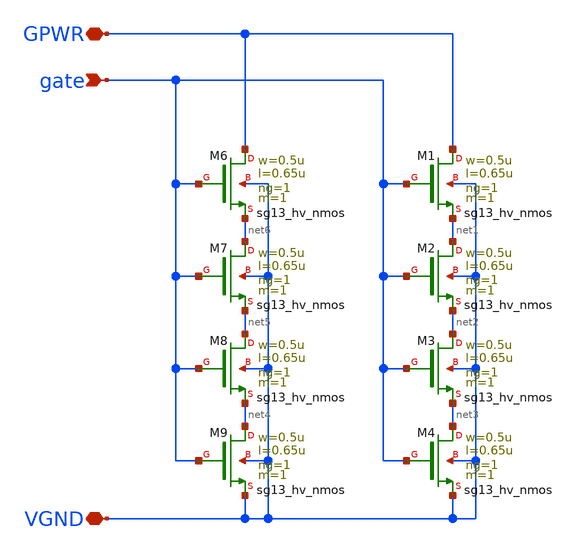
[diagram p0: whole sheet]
** sch_path: ihp-sg13cmos5l/libs.tech/xschem/hm_analog/hv_dischg.sch
**.subckt hv_dischg GPWR VGND gate
*.iopin GPWR
*.iopin VGND
*.ipin gate
XM6 GPWR gate net6 VGND sg13_hv_nmos w=0.5u l=0.65u ng=1 m=1 mm_ok=1
XM7 net6 gate net5 VGND sg13_hv_nmos w=0.5u l=0.65u ng=1 m=1 mm_ok=1
XM8 net5 gate net4 VGND sg13_hv_nmos w=0.5u l=0.65u ng=1 m=1 mm_ok=1
XM9 net4 gate VGND VGND sg13_hv_nmos w=0.5u l=0.65u ng=1 m=1 mm_ok=1
XM1 GPWR gate net1 VGND sg13_hv_nmos w=0.5u l=0.65u ng=1 m=1 mm_ok=1
XM2 net1 gate net2 VGND sg13_hv_nmos w=0.5u l=0.65u ng=1 m=1 mm_ok=1
XM3 net2 gate net3 VGND sg13_hv_nmos w=0.5u l=0.65u ng=1 m=1 mm_ok=1
XM4 net3 gate VGND VGND sg13_hv_nmos w=0.5u l=0.65u ng=1 m=1 mm_ok=1
**.ends
.end
